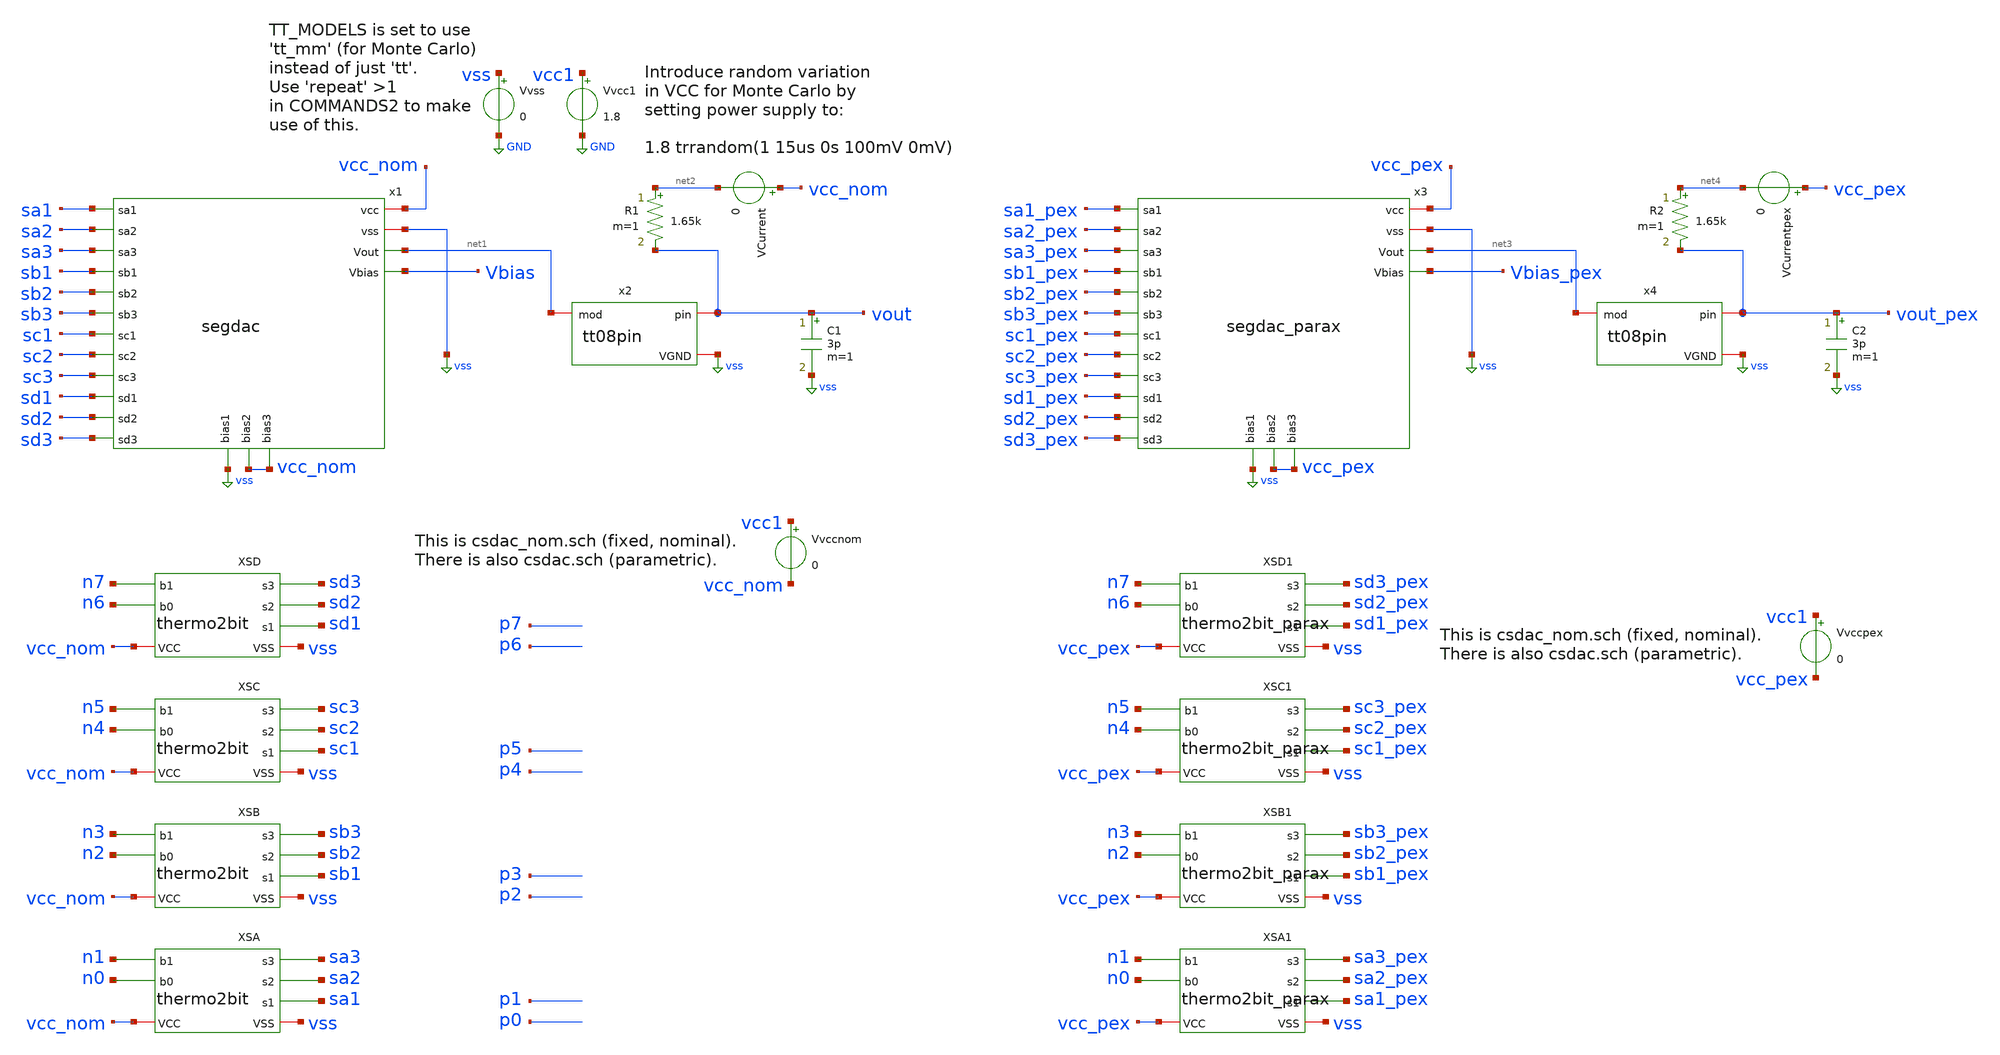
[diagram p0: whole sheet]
** sch_path: xschem/tb_segdac_pex.sch
**.subckt tb_segdac_pex
Vvcc1 vcc1 GND 1.8
Vvss vss GND 0
Vvccnom vcc1 vcc_nom 0
x1 sa1 vcc_nom sa2 vss sa3 net1 sb1 sb2 Vbias sb3 sc1 sc2 sc3 sd1 sd2 sd3 vss vcc_nom vcc_nom segdac
XSA vcc_nom vss sa3 n1 sa2 sa1 n0 thermo2bit
XSB vcc_nom vss sb3 n3 sb2 sb1 n2 thermo2bit
XSC vcc_nom vss sc3 n5 sc2 sc1 n4 thermo2bit
XSD vcc_nom vss sd3 n7 sd2 sd1 n6 thermo2bit
x2 vout net1 vss tt08pin
C1 vout vss 3p m=1
VCurrent vcc_nom net2 0
R1 net2 vout 1.65k m=1
Vvccpex vcc1 vcc_pex 0
x3 sa1_pex vcc_pex sa2_pex vss sa3_pex net3 sb1_pex sb2_pex Vbias_pex sb3_pex sc1_pex sc2_pex
+ sc3_pex sd1_pex sd2_pex sd3_pex vss vcc_pex vcc_pex segdac_parax
XSA1 vcc_pex vss sa3_pex n1 sa2_pex sa1_pex n0 thermo2bit_parax
XSB1 vcc_pex vss sb3_pex n3 sb2_pex sb1_pex n2 thermo2bit_parax
XSC1 vcc_pex vss sc3_pex n5 sc2_pex sc1_pex n4 thermo2bit_parax
XSD1 vcc_pex vss sd3_pex n7 sd2_pex sd1_pex n6 thermo2bit_parax
x4 vout_pex net3 vss tt08pin
C2 vout_pex vss 3p m=1
VCurrentpex vcc_pex net4 0
R2 net4 vout_pex 1.65k m=1
**** begin user architecture code



.param singlebits=0
.IF (singlebits == 1)
* Mode to just test each binary-weighted level:
Vxp0 p0 GND pulse 0v 1.8v 1u 1n 1n 1u 10u
Vxp1 p1 GND pulse 0v 1.8v 2u 1n 1n 1u 10u
Vxp2 p2 GND pulse 0v 1.8v 3u 1n 1n 1u 10u
Vxp3 p3 GND pulse 0v 1.8v 4u 1n 1n 1u 10u
Vxp4 p4 GND pulse 0v 1.8v 5u 1n 1n 1u 10u
Vxp5 p5 GND pulse 0v 1.8v 6u 1n 1n 1u 10u
Vxp6 p6 GND pulse 0v 1.8v 7u 1n 1n 1u 10u
Vxp7 p7 GND pulse 0v 1.8v 8u 1n 1n 1u 10u
Vxn0 n0 GND pulse 1.8v 0v 1u 1n 1n 1u 10u
Vxn1 n1 GND pulse 1.8v 0v 2u 1n 1n 1u 10u
Vxn2 n2 GND pulse 1.8v 0v 3u 1n 1n 1u 10u
Vxn3 n3 GND pulse 1.8v 0v 4u 1n 1n 1u 10u
Vxn4 n4 GND pulse 1.8v 0v 5u 1n 1n 1u 10u
Vxn5 n5 GND pulse 1.8v 0v 6u 1n 1n 1u 10u
Vxn6 n6 GND pulse 1.8v 0v 7u 1n 1n 1u 10u
Vxn7 n7 GND pulse 1.8v 0v 8u 1n 1n 1u 10u
.ELSEIF (singlebits == 0)
* Mode to test full 0..255 trange:
Vxp0 p0 GND pulse 1.8v 0v 0n 1n 1n 39n 80n
Vxp1 p1 GND pulse 1.8v 0v 0n 1n 1n 79n 160n
Vxp2 p2 GND pulse 1.8v 0v 0n 1n 1n 159n 320n
Vxp3 p3 GND pulse 1.8v 0v 0n 1n 1n 319n 640n
Vxp4 p4 GND pulse 1.8v 0v 0n 1n 1n 639n 1280n
Vxp5 p5 GND pulse 1.8v 0v 0n 1n 1n 1279n 2560n
Vxp6 p6 GND pulse 1.8v 0v 0n 1n 1n 2559n 5120n
Vxp7 p7 GND pulse 1.8v 0v 0n 1n 1n 5119n 10240n
Vxn0 n0 GND pulse 0v 1.8v 0n 1n 1n 39n 80n
Vxn1 n1 GND pulse 0v 1.8v 0n 1n 1n 79n 160n
Vxn2 n2 GND pulse 0v 1.8v 0n 1n 1n 159n 320n
Vxn3 n3 GND pulse 0v 1.8v 0n 1n 1n 319n 640n
Vxn4 n4 GND pulse 0v 1.8v 0n 1n 1n 639n 1280n
Vxn5 n5 GND pulse 0v 1.8v 0n 1n 1n 1279n 2560n
Vxn6 n6 GND pulse 0v 1.8v 0n 1n 1n 2559n 5120n
Vxn7 n7 GND pulse 0v 1.8v 0n 1n 1n 5119n 10240n
.ENDIF

.options savecurrents
.control

  * If using Monte Carlo, change to repeat to (say) 5:
  repeat 1
    save all
    tran 1n 12.8u
    write tb_segdac_pex.raw
    + i(vvss) vcc1 vbias vout i(vvccnom) i(vcurrent)
      + p0 p1 p2 p3 p4 p5 p6 p7
      + sa1 sa2 sa3
      + sb1 sb2 sb3
      + sc1 sc2 sc3
      + sd1 sd2 sd3
    + vbias_pex vout_pex i(vvccpex) i(vcurrentpex)
      + p0 p1 p2 p3 p4 p5 p6 p7
      + sa1_pex sa2_pex sa3_pex
      + sb1_pex sb2_pex sb3_pex
      + sc1_pex sc2_pex sc3_pex
      + sd1_pex sd2_pex sd3_pex

    * + i(voutload)
    set appendwrite
    reset
  end

*  save all
*  *reset
*  *alterparam MPW=4
*  *alterparam MMW=4
*  tran 1n 12.8u
*  write 11.raw i(vvcc) i(vvss) vpos vneg vbias

*  set appendwrite
*  alterparam MPW=4
*  alterparam MMW=4
*  reset
*  tran 1n 12.8u
*  write 11.raw i(vvcc) i(vvss) vpos vneg vbias

.endc




.lib $::SKYWATER_MODELS/sky130.lib.spice tt
.include $::SKYWATER_STDCELLS/sky130_fd_sc_hd.spice

**** end user architecture code
**.ends

* expanding   symbol:  segdac.sym # of pins=19
** sym_path: xschem/segdac.sym
** sch_path: xschem/segdac.sch
.subckt segdac sa1 vcc sa2 vss sa3 Vout sb1 sb2 Vbias sb3 sc1 sc2 sc3 sd1 sd2 sd3 bias1 bias2 bias3
*.iopin vcc
*.iopin vss
*.opin Vout
*.opin Vbias
*.ipin sa1
*.ipin sa2
*.ipin sa3
*.ipin sb1
*.ipin sb2
*.ipin sb3
*.ipin sc1
*.ipin sc2
*.ipin sc3
*.ipin sd1
*.ipin sd2
*.ipin sd3
*.ipin bias1
*.ipin bias2
*.ipin bias3
XMmirror Vbias Vbias vss vss sky130_fd_pr__nfet_01v8 L=0.5 W=0.5 nf=1 ad='int((nf+1)/2) * W/nf * 0.29'
+ as='int((nf+2)/2) * W/nf * 0.29' pd='2*int((nf+1)/2) * (W/nf + 0.29)' ps='2*int((nf+2)/2) * (W/nf + 0.29)'
+ nrd='0.29 / W' nrs='0.29 / W' sa=0 sb=0 sd=0 mult=1 m=1
XMia1 net1 Vbias vss vss sky130_fd_pr__nfet_01v8 L=5 W=0.5 nf=1 ad='int((nf+1)/2) * W/nf * 0.29' as='int((nf+2)/2) * W/nf * 0.29'
+ pd='2*int((nf+1)/2) * (W/nf + 0.29)' ps='2*int((nf+2)/2) * (W/nf + 0.29)' nrd='0.29 / W' nrs='0.29 / W'
+ sa=0 sb=0 sd=0 mult=1 m=1
XMia2 net2 Vbias vss vss sky130_fd_pr__nfet_01v8 L=5 W=0.5 nf=1 ad='int((nf+1)/2) * W/nf * 0.29' as='int((nf+2)/2) * W/nf * 0.29'
+ pd='2*int((nf+1)/2) * (W/nf + 0.29)' ps='2*int((nf+2)/2) * (W/nf + 0.29)' nrd='0.29 / W' nrs='0.29 / W'
+ sa=0 sb=0 sd=0 mult=1 m=1
XMia3 net3 Vbias vss vss sky130_fd_pr__nfet_01v8 L=5 W=0.5 nf=1 ad='int((nf+1)/2) * W/nf * 0.29' as='int((nf+2)/2) * W/nf * 0.29'
+ pd='2*int((nf+1)/2) * (W/nf + 0.29)' ps='2*int((nf+2)/2) * (W/nf + 0.29)' nrd='0.29 / W' nrs='0.29 / W'
+ sa=0 sb=0 sd=0 mult=1 m=1
XMsa1 Vout sa1 net1 vss sky130_fd_pr__nfet_01v8 L=0.15 W=0.5 nf=1 ad='int((nf+1)/2) * W/nf * 0.29' as='int((nf+2)/2) * W/nf * 0.29'
+ pd='2*int((nf+1)/2) * (W/nf + 0.29)' ps='2*int((nf+2)/2) * (W/nf + 0.29)' nrd='0.29 / W' nrs='0.29 / W'
+ sa=0 sb=0 sd=0 mult=1 m=1
XMsa2 Vout sa2 net2 vss sky130_fd_pr__nfet_01v8 L=0.15 W=0.5 nf=1 ad='int((nf+1)/2) * W/nf * 0.29' as='int((nf+2)/2) * W/nf * 0.29'
+ pd='2*int((nf+1)/2) * (W/nf + 0.29)' ps='2*int((nf+2)/2) * (W/nf + 0.29)' nrd='0.29 / W' nrs='0.29 / W'
+ sa=0 sb=0 sd=0 mult=1 m=1
XMsa3 Vout sa3 net3 vss sky130_fd_pr__nfet_01v8 L=0.15 W=0.5 nf=1 ad='int((nf+1)/2) * W/nf * 0.29' as='int((nf+2)/2) * W/nf * 0.29'
+ pd='2*int((nf+1)/2) * (W/nf + 0.29)' ps='2*int((nf+2)/2) * (W/nf + 0.29)' nrd='0.29 / W' nrs='0.29 / W'
+ sa=0 sb=0 sd=0 mult=1 m=1
XMib1 net4 Vbias vss vss sky130_fd_pr__nfet_01v8 L=1.2 W=0.5 nf=1 ad='int((nf+1)/2) * W/nf * 0.29' as='int((nf+2)/2) * W/nf * 0.29'
+ pd='2*int((nf+1)/2) * (W/nf + 0.29)' ps='2*int((nf+2)/2) * (W/nf + 0.29)' nrd='0.29 / W' nrs='0.29 / W'
+ sa=0 sb=0 sd=0 mult=1 m=1
XMib2 net5 Vbias vss vss sky130_fd_pr__nfet_01v8 L=1.2 W=0.5 nf=1 ad='int((nf+1)/2) * W/nf * 0.29' as='int((nf+2)/2) * W/nf * 0.29'
+ pd='2*int((nf+1)/2) * (W/nf + 0.29)' ps='2*int((nf+2)/2) * (W/nf + 0.29)' nrd='0.29 / W' nrs='0.29 / W'
+ sa=0 sb=0 sd=0 mult=1 m=1
XMib3 net6 Vbias vss vss sky130_fd_pr__nfet_01v8 L=1.2 W=0.5 nf=1 ad='int((nf+1)/2) * W/nf * 0.29' as='int((nf+2)/2) * W/nf * 0.29'
+ pd='2*int((nf+1)/2) * (W/nf + 0.29)' ps='2*int((nf+2)/2) * (W/nf + 0.29)' nrd='0.29 / W' nrs='0.29 / W'
+ sa=0 sb=0 sd=0 mult=1 m=1
XMsb1 Vout sb1 net4 vss sky130_fd_pr__nfet_01v8 L=0.15 W=1 nf=1 ad='int((nf+1)/2) * W/nf * 0.29' as='int((nf+2)/2) * W/nf * 0.29'
+ pd='2*int((nf+1)/2) * (W/nf + 0.29)' ps='2*int((nf+2)/2) * (W/nf + 0.29)' nrd='0.29 / W' nrs='0.29 / W'
+ sa=0 sb=0 sd=0 mult=1 m=1
XMsb2 Vout sb2 net5 vss sky130_fd_pr__nfet_01v8 L=0.15 W=1 nf=1 ad='int((nf+1)/2) * W/nf * 0.29' as='int((nf+2)/2) * W/nf * 0.29'
+ pd='2*int((nf+1)/2) * (W/nf + 0.29)' ps='2*int((nf+2)/2) * (W/nf + 0.29)' nrd='0.29 / W' nrs='0.29 / W'
+ sa=0 sb=0 sd=0 mult=1 m=1
XMsb3 Vout sb3 net6 vss sky130_fd_pr__nfet_01v8 L=0.15 W=1 nf=1 ad='int((nf+1)/2) * W/nf * 0.29' as='int((nf+2)/2) * W/nf * 0.29'
+ pd='2*int((nf+1)/2) * (W/nf + 0.29)' ps='2*int((nf+2)/2) * (W/nf + 0.29)' nrd='0.29 / W' nrs='0.29 / W'
+ sa=0 sb=0 sd=0 mult=1 m=1
XMic1 net7 Vbias vss vss sky130_fd_pr__nfet_01v8 L=0.5 W=1 nf=1 ad='int((nf+1)/2) * W/nf * 0.29' as='int((nf+2)/2) * W/nf * 0.29'
+ pd='2*int((nf+1)/2) * (W/nf + 0.29)' ps='2*int((nf+2)/2) * (W/nf + 0.29)' nrd='0.29 / W' nrs='0.29 / W'
+ sa=0 sb=0 sd=0 mult=1 m=1
XMic2 net8 Vbias vss vss sky130_fd_pr__nfet_01v8 L=0.5 W=1 nf=1 ad='int((nf+1)/2) * W/nf * 0.29' as='int((nf+2)/2) * W/nf * 0.29'
+ pd='2*int((nf+1)/2) * (W/nf + 0.29)' ps='2*int((nf+2)/2) * (W/nf + 0.29)' nrd='0.29 / W' nrs='0.29 / W'
+ sa=0 sb=0 sd=0 mult=1 m=1
XMic3 net9 Vbias vss vss sky130_fd_pr__nfet_01v8 L=0.5 W=1 nf=1 ad='int((nf+1)/2) * W/nf * 0.29' as='int((nf+2)/2) * W/nf * 0.29'
+ pd='2*int((nf+1)/2) * (W/nf + 0.29)' ps='2*int((nf+2)/2) * (W/nf + 0.29)' nrd='0.29 / W' nrs='0.29 / W'
+ sa=0 sb=0 sd=0 mult=1 m=1
XMsc1 Vout sc1 net7 vss sky130_fd_pr__nfet_01v8 L=0.15 W=1.4 nf=1 ad='int((nf+1)/2) * W/nf * 0.29' as='int((nf+2)/2) * W/nf * 0.29'
+ pd='2*int((nf+1)/2) * (W/nf + 0.29)' ps='2*int((nf+2)/2) * (W/nf + 0.29)' nrd='0.29 / W' nrs='0.29 / W'
+ sa=0 sb=0 sd=0 mult=1 m=1
XMsc2 Vout sc2 net8 vss sky130_fd_pr__nfet_01v8 L=0.15 W=1.4 nf=1 ad='int((nf+1)/2) * W/nf * 0.29' as='int((nf+2)/2) * W/nf * 0.29'
+ pd='2*int((nf+1)/2) * (W/nf + 0.29)' ps='2*int((nf+2)/2) * (W/nf + 0.29)' nrd='0.29 / W' nrs='0.29 / W'
+ sa=0 sb=0 sd=0 mult=1 m=1
XMsc3 Vout sc3 net9 vss sky130_fd_pr__nfet_01v8 L=0.15 W=1.4 nf=1 ad='int((nf+1)/2) * W/nf * 0.29' as='int((nf+2)/2) * W/nf * 0.29'
+ pd='2*int((nf+1)/2) * (W/nf + 0.29)' ps='2*int((nf+2)/2) * (W/nf + 0.29)' nrd='0.29 / W' nrs='0.29 / W'
+ sa=0 sb=0 sd=0 mult=1 m=1
XMid1 net10 Vbias vss vss sky130_fd_pr__nfet_01v8 L=0.3 W=2.6 nf=1 ad='int((nf+1)/2) * W/nf * 0.29' as='int((nf+2)/2) * W/nf * 0.29'
+ pd='2*int((nf+1)/2) * (W/nf + 0.29)' ps='2*int((nf+2)/2) * (W/nf + 0.29)' nrd='0.29 / W' nrs='0.29 / W'
+ sa=0 sb=0 sd=0 mult=1 m=1
XMid2 net11 Vbias vss vss sky130_fd_pr__nfet_01v8 L=0.3 W=2.6 nf=1 ad='int((nf+1)/2) * W/nf * 0.29' as='int((nf+2)/2) * W/nf * 0.29'
+ pd='2*int((nf+1)/2) * (W/nf + 0.29)' ps='2*int((nf+2)/2) * (W/nf + 0.29)' nrd='0.29 / W' nrs='0.29 / W'
+ sa=0 sb=0 sd=0 mult=1 m=1
XMid3 net12 Vbias vss vss sky130_fd_pr__nfet_01v8 L=0.3 W=2.6 nf=1 ad='int((nf+1)/2) * W/nf * 0.29' as='int((nf+2)/2) * W/nf * 0.29'
+ pd='2*int((nf+1)/2) * (W/nf + 0.29)' ps='2*int((nf+2)/2) * (W/nf + 0.29)' nrd='0.29 / W' nrs='0.29 / W'
+ sa=0 sb=0 sd=0 mult=1 m=1
XMsd1 Vout sd1 net10 vss sky130_fd_pr__nfet_01v8 L=0.2 W=3.3 nf=1 ad='int((nf+1)/2) * W/nf * 0.29' as='int((nf+2)/2) * W/nf * 0.29'
+ pd='2*int((nf+1)/2) * (W/nf + 0.29)' ps='2*int((nf+2)/2) * (W/nf + 0.29)' nrd='0.29 / W' nrs='0.29 / W'
+ sa=0 sb=0 sd=0 mult=1 m=1
XMsd2 Vout sd2 net11 vss sky130_fd_pr__nfet_01v8 L=0.2 W=3.3 nf=1 ad='int((nf+1)/2) * W/nf * 0.29' as='int((nf+2)/2) * W/nf * 0.29'
+ pd='2*int((nf+1)/2) * (W/nf + 0.29)' ps='2*int((nf+2)/2) * (W/nf + 0.29)' nrd='0.29 / W' nrs='0.29 / W'
+ sa=0 sb=0 sd=0 mult=1 m=1
XMsd3 Vout sd3 net12 vss sky130_fd_pr__nfet_01v8 L=0.2 W=3.3 nf=1 ad='int((nf+1)/2) * W/nf * 0.29' as='int((nf+2)/2) * W/nf * 0.29'
+ pd='2*int((nf+1)/2) * (W/nf + 0.29)' ps='2*int((nf+2)/2) * (W/nf + 0.29)' nrd='0.29 / W' nrs='0.29 / W'
+ sa=0 sb=0 sd=0 mult=1 m=1
XM1 Vbias bias1 vcc vcc sky130_fd_pr__pfet_01v8 L=0.5 W=0.5 nf=1 ad='int((nf+1)/2) * W/nf * 0.29' as='int((nf+2)/2) * W/nf * 0.29'
+ pd='2*int((nf+1)/2) * (W/nf + 0.29)' ps='2*int((nf+2)/2) * (W/nf + 0.29)' nrd='0.29 / W' nrs='0.29 / W'
+ sa=0 sb=0 sd=0 mult=1 m=1
XM2 Vbias bias2 vcc vcc sky130_fd_pr__pfet_01v8 L=1 W=0.5 nf=1 ad='int((nf+1)/2) * W/nf * 0.29' as='int((nf+2)/2) * W/nf * 0.29'
+ pd='2*int((nf+1)/2) * (W/nf + 0.29)' ps='2*int((nf+2)/2) * (W/nf + 0.29)' nrd='0.29 / W' nrs='0.29 / W'
+ sa=0 sb=0 sd=0 mult=1 m=1
XM3 Vbias bias3 vcc vcc sky130_fd_pr__pfet_01v8 L=2 W=0.5 nf=1 ad='int((nf+1)/2) * W/nf * 0.29' as='int((nf+2)/2) * W/nf * 0.29'
+ pd='2*int((nf+1)/2) * (W/nf + 0.29)' ps='2*int((nf+2)/2) * (W/nf + 0.29)' nrd='0.29 / W' nrs='0.29 / W'
+ sa=0 sb=0 sd=0 mult=1 m=1
.ends


* expanding   symbol:  thermo2bit.sym # of pins=7
** sym_path: xschem/thermo2bit.sym
** sch_path: xschem/thermo2bit.sch
.subckt thermo2bit VCC VSS s3 b1 s2 s1 b0
*.ipin b1
*.opin s2
*.ipin b0
*.opin s1
*.opin s3
*.iopin VCC
*.iopin VSS
x2 b0 b1 VSS VSS VCC VCC s3 sky130_fd_sc_hd__and2_1
x3 b1 b0 VSS VSS VCC VCC s1 sky130_fd_sc_hd__or2_1
R1 s2 b1 0 m=1
.ends


* expanding   symbol:  tt08pin.sym # of pins=3
** sym_path: xschem/tt08pin.sym
** sch_path: xschem/tt08pin.sch
.subckt tt08pin pin mod VGND
*.iopin pin
*.iopin VGND
*.iopin mod
R1 net1 pin 1 m=1
C1 pin VGND 1p m=1
L1 net2 net1 1n m=1
V1 VAPWR VGND 3.3
C2 net2 VGND 2p m=1
R2 net3 net2 50 m=1
XM2 net3 VGND mod VAPWR sky130_fd_pr__pfet_g5v0d10v5 L=0.5 W=100 nf=20 ad='int((nf+1)/2) * W/nf * 0.29'
+ as='int((nf+2)/2) * W/nf * 0.29' pd='2*int((nf+1)/2) * (W/nf + 0.29)' ps='2*int((nf+2)/2) * (W/nf + 0.29)'
+ nrd='0.29 / W' nrs='0.29 / W' sa=0 sb=0 sd=0 mult=1 m=1
XM1 net3 VAPWR mod VGND sky130_fd_pr__nfet_g5v0d10v5 L=0.5 W=60 nf=12 ad='int((nf+1)/2) * W/nf * 0.29'
+ as='int((nf+2)/2) * W/nf * 0.29' pd='2*int((nf+1)/2) * (W/nf + 0.29)' ps='2*int((nf+2)/2) * (W/nf + 0.29)'
+ nrd='0.29 / W' nrs='0.29 / W' sa=0 sb=0 sd=0 mult=1 m=1
XM4 net3 VAPWR VGND VAPWR sky130_fd_pr__pfet_g5v0d10v5 L=0.5 W=100 nf=20 ad='int((nf+1)/2) * W/nf * 0.29'
+ as='int((nf+2)/2) * W/nf * 0.29' pd='2*int((nf+1)/2) * (W/nf + 0.29)' ps='2*int((nf+2)/2) * (W/nf + 0.29)'
+ nrd='0.29 / W' nrs='0.29 / W' sa=0 sb=0 sd=0 mult=15 m=15
XM3 net3 VGND VGND VGND sky130_fd_pr__nfet_g5v0d10v5 L=0.5 W=60 nf=12 ad='int((nf+1)/2) * W/nf * 0.29'
+ as='int((nf+2)/2) * W/nf * 0.29' pd='2*int((nf+1)/2) * (W/nf + 0.29)' ps='2*int((nf+2)/2) * (W/nf + 0.29)'
+ nrd='0.29 / W' nrs='0.29 / W' sa=0 sb=0 sd=0 mult=15 m=15
C3 mod VGND 250f m=1
.ends


* expanding   symbol:  segdac_parax.sym # of pins=19
** sym_path: xschem/segdac.sym
.include [file normalize ../mag/segdac.sim.spice]

* expanding   symbol:  thermo2bit_parax.sym # of pins=7
** sym_path: xschem/thermo2bit.sym
.include [file normalize ../mag/thermo2bit.sim.spice]
.GLOBAL GND
.GLOBAL vss
.GLOBAL VGND
.GLOBAL VAPWR
.end
